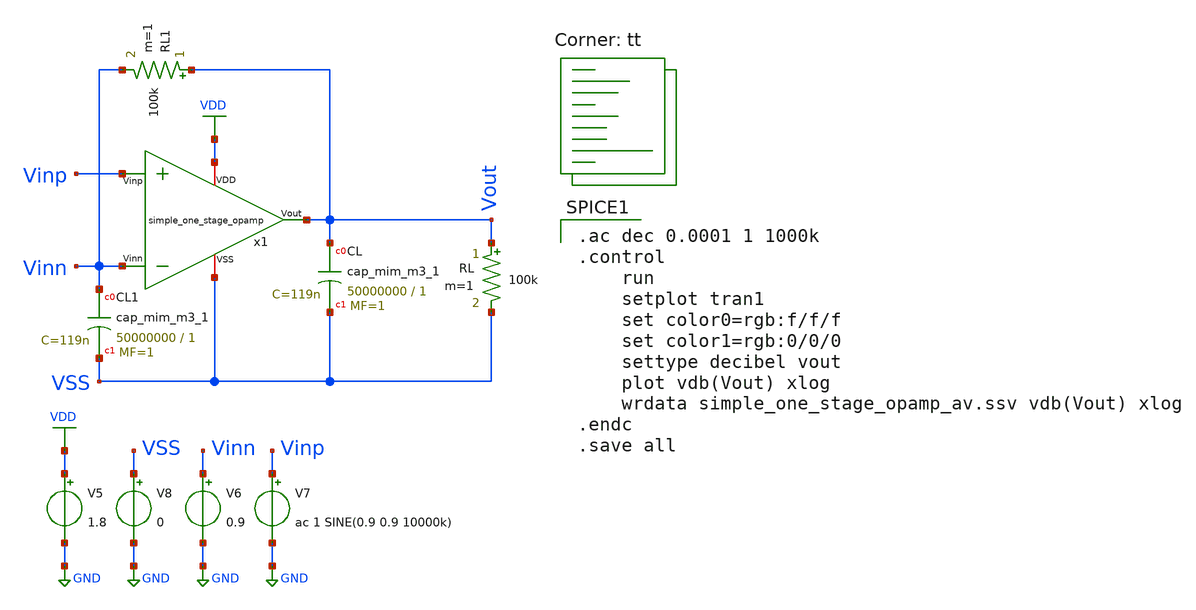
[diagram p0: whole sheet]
** sch_path: opamp_design/simple_one_stage_opamp/simple_one_stage_opamp_av.sch
**.subckt simple_one_stage_opamp_av
XCL Vout VSS sky130_fd_pr__cap_mim_m3_1 W=50000000 L=1 MF=1 m=1
RL Vout VSS 100k m=1
XCL1 Vinn VSS sky130_fd_pr__cap_mim_m3_1 W=50000000 L=1 MF=1 m=1
RL1 Vout Vinn 100k m=1
V5 VDD GND 1.8
V6 Vinn GND 0.9
V7 Vinp GND ac 1 SINE(0.9 0.9 10000k)
V8 VSS GND 0
x1 VDD Vout Vinp Vinn VSS simple_one_stage_opamp
**** begin user architecture code

.ac dec 0.0001 1 1000k
.control
	run
	setplot tran1
	set color0=rgb:f/f/f
	set color1=rgb:0/0/0
	settype decibel vout
	plot vdb(Vout) xlog
	wrdata simple_one_stage_opamp_av.ssv vdb(Vout) xlog
.endc
.save all


.lib $::SKYWATER_MODELS/sky130.lib.spice tt
**** end user architecture code
**.ends

* expanding   symbol:
*+  /home/ricardoatt/RATT_repos/Proyectos_xschem/opamp_design/simple_one_stage_opamp/simple_one_stage_opamp.sym # of pins=5
** sym_path: opamp_design/simple_one_stage_opamp/simple_one_stage_opamp.sym
** sch_path: opamp_design/simple_one_stage_opamp/simple_one_stage_opamp.sch
.subckt simple_one_stage_opamp VDD Vout Vinp Vinn VSS
*.iopin VSS
*.iopin VDD
*.ipin Vinp
*.ipin Vinn
*.opin Vout
XM1 net2 Vinp net1 VSS sky130_fd_pr__nfet_01v8 L=0.15 W=15.648 nf=1 ad='int((nf+1)/2) * W/nf * 0.29'
+ as='int((nf+2)/2) * W/nf * 0.29' pd='2*int((nf+1)/2) * (W/nf + 0.29)' ps='2*int((nf+2)/2) * (W/nf + 0.29)'
+ nrd='0.29 / W' nrs='0.29 / W' sa=0 sb=0 sd=0 mult=1 m=1
XM4 net2 net2 VDD VDD sky130_fd_pr__pfet_01v8 L=0.15 W=0.449 nf=1 ad='int((nf+1)/2) * W/nf * 0.29' as='int((nf+2)/2) * W/nf * 0.29'
+ pd='2*int((nf+1)/2) * (W/nf + 0.29)' ps='2*int((nf+2)/2) * (W/nf + 0.29)' nrd='0.29 / W' nrs='0.29 / W'
+ sa=0 sb=0 sd=0 mult=1 m=1
XM2 Vout Vinn net1 VSS sky130_fd_pr__nfet_01v8 L=0.15 W=15.648 nf=1 ad='int((nf+1)/2) * W/nf * 0.29'
+ as='int((nf+2)/2) * W/nf * 0.29' pd='2*int((nf+1)/2) * (W/nf + 0.29)' ps='2*int((nf+2)/2) * (W/nf + 0.29)'
+ nrd='0.29 / W' nrs='0.29 / W' sa=0 sb=0 sd=0 mult=1 m=1
XM3 Vout net2 VDD VDD sky130_fd_pr__pfet_01v8 L=0.15 W=0.449 nf=1 ad='int((nf+1)/2) * W/nf * 0.29' as='int((nf+2)/2) * W/nf * 0.29'
+ pd='2*int((nf+1)/2) * (W/nf + 0.29)' ps='2*int((nf+2)/2) * (W/nf + 0.29)' nrd='0.29 / W' nrs='0.29 / W'
+ sa=0 sb=0 sd=0 mult=1 m=1
XM5 net1 net3 VSS VSS sky130_fd_pr__nfet_01v8 L=0.15 W=5.193 nf=1 ad='int((nf+1)/2) * W/nf * 0.29' as='int((nf+2)/2) * W/nf * 0.29'
+ pd='2*int((nf+1)/2) * (W/nf + 0.29)' ps='2*int((nf+2)/2) * (W/nf + 0.29)' nrd='0.29 / W' nrs='0.29 / W'
+ sa=0 sb=0 sd=0 mult=1 m=1
XM6 net3 net3 VSS VSS sky130_fd_pr__nfet_01v8 L=0.15 W=5.193 nf=1 ad='int((nf+1)/2) * W/nf * 0.29' as='int((nf+2)/2) * W/nf * 0.29'
+ pd='2*int((nf+1)/2) * (W/nf + 0.29)' ps='2*int((nf+2)/2) * (W/nf + 0.29)' nrd='0.29 / W' nrs='0.29 / W'
+ sa=0 sb=0 sd=0 mult=1 m=1
I0 VDD net3 48u
.ends

.GLOBAL VDD
.GLOBAL GND
.end
